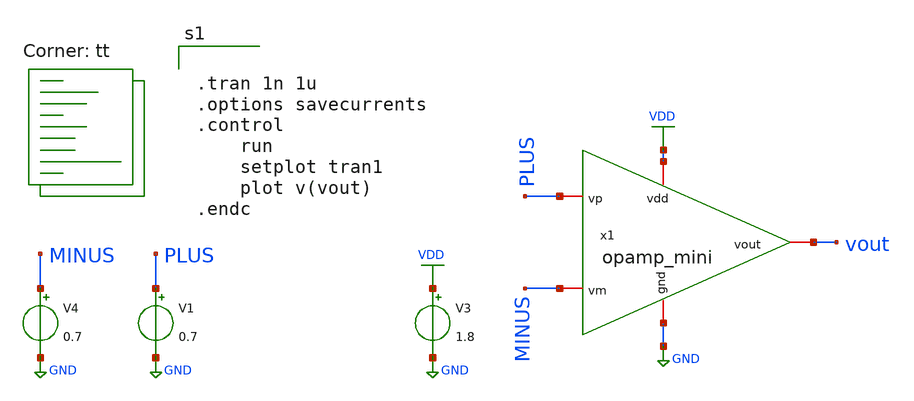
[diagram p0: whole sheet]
** sch_path: OPAMP/tb_opamp_mini.sch
**.subckt tb_opamp_mini
x1 VDD vout MINUS PLUS GND opamp_mini
V1 PLUS GND 0.7
V3 VDD GND 1.8
V4 MINUS GND 0.7
**** begin user architecture code
.lib $::SKYWATER_MODELS/sky130.lib.spice tt


.tran 1n 1u
.options savecurrents
.control
	run
	setplot tran1
	plot v(vout)
.endc



**** end user architecture code
**.ends

* expanding   symbol:  /home/alex/Desktop/EDA/SNN_IPN/opamp_mini/opamp_mini.sym # of pins=5
** sym_path: OPAMP/opamp_mini.sym
** sch_path: OPAMP/opamp_mini.sch
.subckt opamp_mini vdd vout vm vp gnd
*.iopin vdd
*.iopin gnd
*.iopin vout
*.iopin vm
*.iopin vp
XM1 vout vb2 vdd vdd sky130_fd_pr__pfet_01v8 L=0.8 W=4 nf=1 ad='int((nf+1)/2) * W/nf * 0.29' as='int((nf+2)/2) * W/nf * 0.29'
+ pd='2*int((nf+1)/2) * (W/nf + 0.29)' ps='2*int((nf+2)/2) * (W/nf + 0.29)' nrd='0.29 / W' nrs='0.29 / W'
+ sa=0 sb=0 sd=0 mult=1 m=1
XM2 vb2 vb2 vdd vdd sky130_fd_pr__pfet_01v8 L=0.8 W=4 nf=1 ad='int((nf+1)/2) * W/nf * 0.29' as='int((nf+2)/2) * W/nf * 0.29'
+ pd='2*int((nf+1)/2) * (W/nf + 0.29)' ps='2*int((nf+2)/2) * (W/nf + 0.29)' nrd='0.29 / W' nrs='0.29 / W'
+ sa=0 sb=0 sd=0 mult=1 m=1
XM3 vb2 vp net1 gnd sky130_fd_pr__nfet_01v8 L=0.3 W=2 nf=1 ad='int((nf+1)/2) * W/nf * 0.29' as='int((nf+2)/2) * W/nf * 0.29'
+ pd='2*int((nf+1)/2) * (W/nf + 0.29)' ps='2*int((nf+2)/2) * (W/nf + 0.29)' nrd='0.29 / W' nrs='0.29 / W'
+ sa=0 sb=0 sd=0 mult=1 m=1
XM4 vout vm net1 gnd sky130_fd_pr__nfet_01v8 L=0.3 W=2 nf=1 ad='int((nf+1)/2) * W/nf * 0.29' as='int((nf+2)/2) * W/nf * 0.29'
+ pd='2*int((nf+1)/2) * (W/nf + 0.29)' ps='2*int((nf+2)/2) * (W/nf + 0.29)' nrd='0.29 / W' nrs='0.29 / W'
+ sa=0 sb=0 sd=0 mult=1 m=1
XM5 net1 vb1 gnd gnd sky130_fd_pr__nfet_01v8 L=1.2 W=0.7 nf=1 ad='int((nf+1)/2) * W/nf * 0.29' as='int((nf+2)/2) * W/nf * 0.29'
+ pd='2*int((nf+1)/2) * (W/nf + 0.29)' ps='2*int((nf+2)/2) * (W/nf + 0.29)' nrd='0.29 / W' nrs='0.29 / W'
+ sa=0 sb=0 sd=0 mult=1 m=1
R1 vdd vb1 1k m=1
R2 vb1 gnd 1k m=1
.ends

.GLOBAL GND
.GLOBAL VDD
.end
